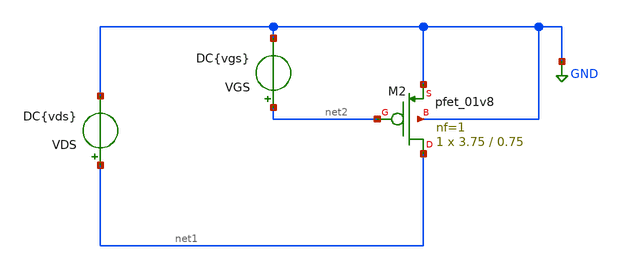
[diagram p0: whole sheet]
** sch_path: Tp1/Simulaciones Profesor/tp1_2.sch
**.subckt tp1_2
VDS net1 GND DC{vds}
XM2 net1 net2 GND GND sky130_fd_pr__pfet_01v8 L=0.75 W=3.75 nf=1 ad='int((nf+1)/2) * W/nf * 0.29' as='int((nf+2)/2) * W/nf * 0.29'
+ pd='2*int((nf+1)/2) * (W/nf + 0.29)' ps='2*int((nf+2)/2) * (W/nf + 0.29)' nrd='0.29 / W' nrs='0.29 / W'
+ sa=0 sb=0 sd=0 mult=1 m=1
VGS net2 GND DC{vgs}
**** begin user architecture code



* Parameters
.param vds = -1.8
.param vgs = -0.9
.options TEMPS = 27.0

* Models
.lib ~/skywater/skywater-pdk/libraries/sky130_fd_pr_ngspice/latest/models/corners/sky130.lib TT

* Data to save
.save all  @M.XM2.msky130_fd_pr__pfet_01v8[id]  @M.XM2.msky130_fd_pr__pfet_01v8[gm]  @M.XM2.msky130_fd_pr__pfet_01v8[vth]  @M.XM2.msky130_fd_pr__pfet_01v8[vds]  @M.XM2.msky130_fd_pr__pfet_01v8[vdsat]  @M.XM2.msky130_fd_pr__pfet_01v8[vgs]

* Simulation
.control
  dc VDS 0 -1.8 -0.01 VGS 0 -1.8 -0.3
  setplot dc1
  plot -1*@M.XM2.msky130_fd_pr__pfet_01v8[id] ylabel Id xlabel Vds title 'Id vs Vds vs Vgs'
  set filetype = ascii
  write tp1_2_dc1.raw

  reset
  dc VGS 0 -1.8 -0.01
  setplot dc2
  plot -1*@M.XM2.msky130_fd_pr__pfet_01v8[id] ylabel Id xlabel Vgs
  set filetype = ascii
  write tp1_2_dc2.raw

.endc

.end


**** end user architecture code
**.ends
.GLOBAL GND
.end
